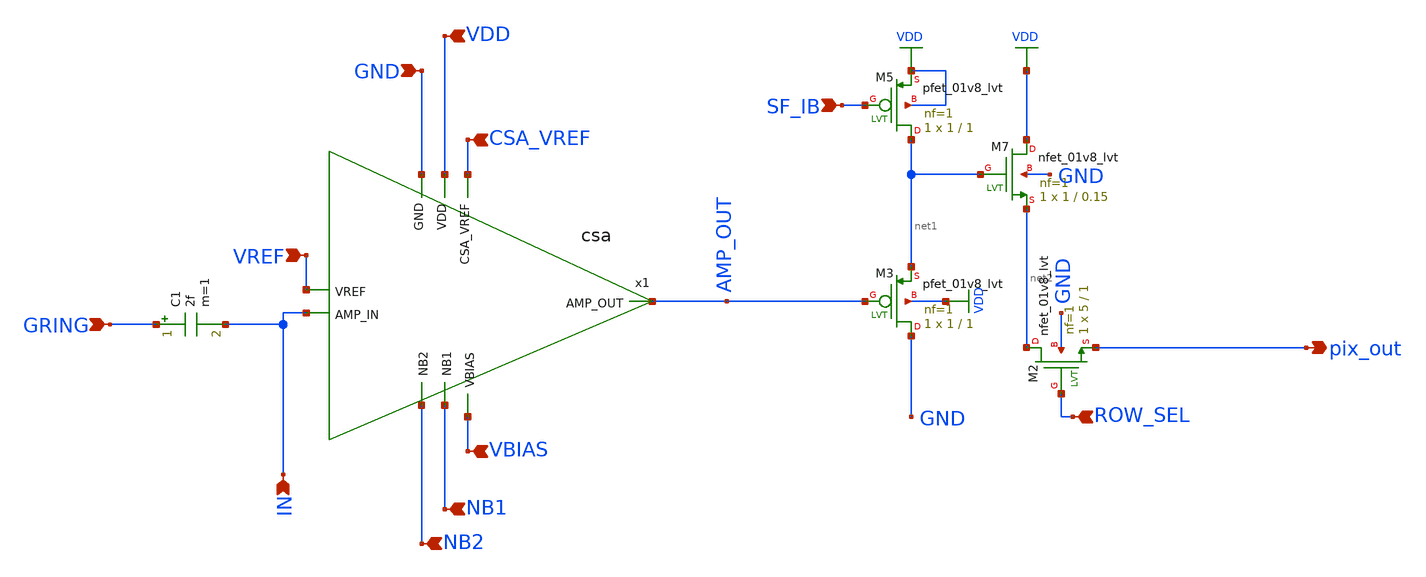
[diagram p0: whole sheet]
** sch_path: xschem/pixel.sch
**.subckt pixel GND VDD CSA_VREF VBIAS NB1 NB2 VREF IN GRING pix_out SF_IB ROW_SEL
*.ipin GND
*.ipin VDD
*.ipin CSA_VREF
*.ipin VBIAS
*.ipin NB1
*.ipin NB2
*.ipin VREF
*.ipin IN
*.ipin GRING
*.opin pix_out
*.ipin SF_IB
*.ipin ROW_SEL
x1 VDD GND AMP_OUT VBIAS VREF IN NB2 NB1 CSA_VREF csa
C1 GRING IN 2f m=1
XM2 net2 ROW_SEL pix_out GND sky130_fd_pr__nfet_01v8_lvt L=1 W=5 nf=1 ad='int((nf+1)/2) * W/nf * 0.29'
+ as='int((nf+2)/2) * W/nf * 0.29' pd='2*int((nf+1)/2) * (W/nf + 0.29)' ps='2*int((nf+2)/2) * (W/nf + 0.29)'
+ nrd='0.29 / W' nrs='0.29 / W' sa=0 sb=0 sd=0 mult=1 m=1
XM3 GND AMP_OUT net1 VDD sky130_fd_pr__pfet_01v8_lvt L=1 W=1 nf=1 ad='int((nf+1)/2) * W/nf * 0.29' as='int((nf+2)/2) * W/nf * 0.29'
+ pd='2*int((nf+1)/2) * (W/nf + 0.29)' ps='2*int((nf+2)/2) * (W/nf + 0.29)' nrd='0.29 / W' nrs='0.29 / W'
+ sa=0 sb=0 sd=0 mult=1 m=1
XM5 net1 SF_IB VDD VDD sky130_fd_pr__pfet_01v8_lvt L=1 W=1 nf=1 ad='int((nf+1)/2) * W/nf * 0.29' as='int((nf+2)/2) * W/nf * 0.29'
+ pd='2*int((nf+1)/2) * (W/nf + 0.29)' ps='2*int((nf+2)/2) * (W/nf + 0.29)' nrd='0.29 / W' nrs='0.29 / W'
+ sa=0 sb=0 sd=0 mult=1 m=1
XM7 VDD net1 net2 GND sky130_fd_pr__nfet_01v8_lvt L=0.15 W=1 nf=1 ad='int((nf+1)/2) * W/nf * 0.29' as='int((nf+2)/2) * W/nf * 0.29'
+ pd='2*int((nf+1)/2) * (W/nf + 0.29)' ps='2*int((nf+2)/2) * (W/nf + 0.29)' nrd='0.29 / W' nrs='0.29 / W'
+ sa=0 sb=0 sd=0 mult=1 m=1
**.ends

* expanding   symbol:  /home/damic/CMOS/TopmetalSe/Pixel/Schematic/csa.sym # of pins=9
** sym_path: xschem/csa.sym
** sch_path: xschem/csa.sch
.subckt csa VDD GND AMP_OUT VBIAS VREF AMP_IN NB2 NB1 CSA_VREF
*.ipin VREF
*.ipin AMP_IN
*.ipin NB1
*.ipin CSA_VREF
*.ipin VBIAS
*.opin AMP_OUT
*.ipin NB2
*.ipin VDD
*.ipin GND
XM2 VDD net4 AMP_OUT GND sky130_fd_pr__nfet_01v8_lvt L=1 W=1 nf=1 ad='int((nf+1)/2) * W/nf * 0.29' as='int((nf+2)/2) * W/nf * 0.29'
+ pd='2*int((nf+1)/2) * (W/nf + 0.29)' ps='2*int((nf+2)/2) * (W/nf + 0.29)' nrd='0.29 / W' nrs='0.29 / W'
+ sa=0 sb=0 sd=0 mult=1 m=1
XM8 net3 net3 net5 VDD sky130_fd_pr__pfet_01v8_lvt L=2 W=1 nf=1 ad='int((nf+1)/2) * W/nf * 0.29' as='int((nf+2)/2) * W/nf * 0.29'
+ pd='2*int((nf+1)/2) * (W/nf + 0.29)' ps='2*int((nf+2)/2) * (W/nf + 0.29)' nrd='0.29 / W' nrs='0.29 / W'
+ sa=0 sb=0 sd=0 mult=1 m=1
XM10 net6 net5 VDD VDD sky130_fd_pr__pfet_01v8_lvt L=1 W=1 nf=1 ad='int((nf+1)/2) * W/nf * 0.29' as='int((nf+2)/2) * W/nf * 0.29'
+ pd='2*int((nf+1)/2) * (W/nf + 0.29)' ps='2*int((nf+2)/2) * (W/nf + 0.29)' nrd='0.29 / W' nrs='0.29 / W'
+ sa=0 sb=0 sd=0 mult=1 m=1
XM11 net5 net5 VDD VDD sky130_fd_pr__pfet_01v8_lvt L=1 W=1 nf=1 ad='int((nf+1)/2) * W/nf * 0.29' as='int((nf+2)/2) * W/nf * 0.29'
+ pd='2*int((nf+1)/2) * (W/nf + 0.29)' ps='2*int((nf+2)/2) * (W/nf + 0.29)' nrd='0.29 / W' nrs='0.29 / W'
+ sa=0 sb=0 sd=0 mult=1 m=1
XM15 AMP_OUT NB2 GND GND sky130_fd_pr__nfet_01v8_lvt L=1.2 W=1 nf=1 ad='int((nf+1)/2) * W/nf * 0.29'
+ as='int((nf+2)/2) * W/nf * 0.29' pd='2*int((nf+1)/2) * (W/nf + 0.29)' ps='2*int((nf+2)/2) * (W/nf + 0.29)'
+ nrd='0.29 / W' nrs='0.29 / W' sa=0 sb=0 sd=0 mult=1 m=1
XM16 net2 NB1 GND GND sky130_fd_pr__nfet_01v8_lvt L=1 W=1.2 nf=1 ad='int((nf+1)/2) * W/nf * 0.29' as='int((nf+2)/2) * W/nf * 0.29'
+ pd='2*int((nf+1)/2) * (W/nf + 0.29)' ps='2*int((nf+2)/2) * (W/nf + 0.29)' nrd='0.29 / W' nrs='0.29 / W'
+ sa=0 sb=0 sd=0 mult=1 m=1
XC3 AMP_IN AMP_OUT sky130_fd_pr__cap_mim_m3_1 W=2 L=2 MF=1 m=1
XM4 net1 VREF net2 GND sky130_fd_pr__nfet_01v8_lvt L=0.15 W=7 nf=1 ad='int((nf+1)/2) * W/nf * 0.29' as='int((nf+2)/2) * W/nf * 0.29'
+ pd='2*int((nf+1)/2) * (W/nf + 0.29)' ps='2*int((nf+2)/2) * (W/nf + 0.29)' nrd='0.29 / W' nrs='0.29 / W'
+ sa=0 sb=0 sd=0 mult=1 m=1
XM7 AMP_IN CSA_VREF AMP_OUT VDD sky130_fd_pr__pfet_01v8_lvt L=7.95 W=0.42 nf=1 ad='int((nf+1)/2) * W/nf * 0.29'
+ as='int((nf+2)/2) * W/nf * 0.29' pd='2*int((nf+1)/2) * (W/nf + 0.29)' ps='2*int((nf+2)/2) * (W/nf + 0.29)'
+ nrd='0.29 / W' nrs='0.29 / W' sa=0 sb=0 sd=0 mult=1 m=1
XM5 net4 net3 net6 VDD sky130_fd_pr__pfet_01v8_lvt L=2 W=1 nf=1 ad='int((nf+1)/2) * W/nf * 0.29' as='int((nf+2)/2) * W/nf * 0.29'
+ pd='2*int((nf+1)/2) * (W/nf + 0.29)' ps='2*int((nf+2)/2) * (W/nf + 0.29)' nrd='0.29 / W' nrs='0.29 / W'
+ sa=0 sb=0 sd=0 mult=1 m=1
XM1 net3 VBIAS net1 GND sky130_fd_pr__nfet_01v8_lvt L=0.8 W=1 nf=1 ad='int((nf+1)/2) * W/nf * 0.29' as='int((nf+2)/2) * W/nf * 0.29'
+ pd='2*int((nf+1)/2) * (W/nf + 0.29)' ps='2*int((nf+2)/2) * (W/nf + 0.29)' nrd='0.29 / W' nrs='0.29 / W'
+ sa=0 sb=0 sd=0 mult=1 m=1
XM3 net7 AMP_IN net2 GND sky130_fd_pr__nfet_01v8_lvt L=0.15 W=7 nf=1 ad='int((nf+1)/2) * W/nf * 0.29'
+ as='int((nf+2)/2) * W/nf * 0.29' pd='2*int((nf+1)/2) * (W/nf + 0.29)' ps='2*int((nf+2)/2) * (W/nf + 0.29)'
+ nrd='0.29 / W' nrs='0.29 / W' sa=0 sb=0 sd=0 mult=1 m=1
XM6 net4 VBIAS net7 GND sky130_fd_pr__nfet_01v8_lvt L=0.8 W=1 nf=1 ad='int((nf+1)/2) * W/nf * 0.29' as='int((nf+2)/2) * W/nf * 0.29'
+ pd='2*int((nf+1)/2) * (W/nf + 0.29)' ps='2*int((nf+2)/2) * (W/nf + 0.29)' nrd='0.29 / W' nrs='0.29 / W'
+ sa=0 sb=0 sd=0 mult=1 m=1
.ends

.GLOBAL VDD
.GLOBAL GND
.end
